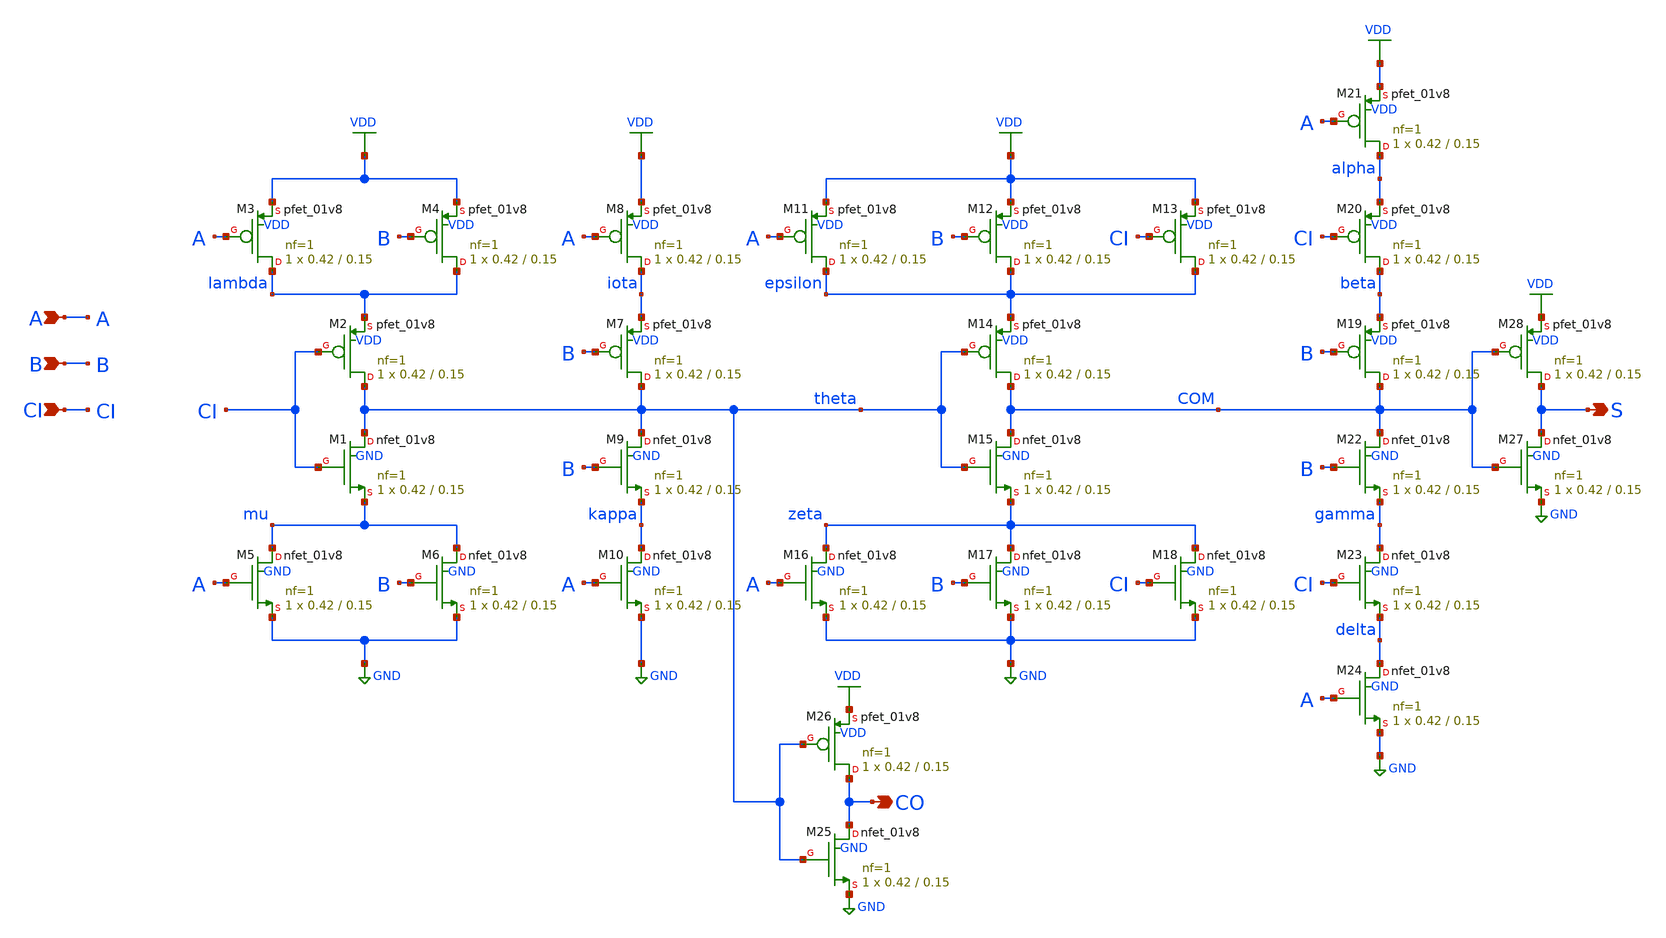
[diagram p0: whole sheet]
** sch_path: xschem/addf.sch
**.subckt addf A B CI S CO
*.ipin A
*.ipin B
*.ipin CI
*.opin S
*.opin CO
XM1 theta CI mu GND sky130_fd_pr__nfet_01v8 L=0.15 W=0.42 nf=1 ad='int((nf+1)/2) * W/nf * 0.29' as='int((nf+2)/2) * W/nf * 0.29'
+ pd='2*int((nf+1)/2) * (W/nf + 0.29)' ps='2*int((nf+2)/2) * (W/nf + 0.29)' nrd='0.29 / W' nrs='0.29 / W'
+ sa=0 sb=0 sd=0 mult=1 m=1
XM2 theta CI lambda VDD sky130_fd_pr__pfet_01v8 L=0.15 W=0.42 nf=1 ad='int((nf+1)/2) * W/nf * 0.29' as='int((nf+2)/2) * W/nf * 0.29'
+ pd='2*int((nf+1)/2) * (W/nf + 0.29)' ps='2*int((nf+2)/2) * (W/nf + 0.29)' nrd='0.29 / W' nrs='0.29 / W'
+ sa=0 sb=0 sd=0 mult=1 m=1
XM3 lambda A VDD VDD sky130_fd_pr__pfet_01v8 L=0.15 W=0.42 nf=1 ad='int((nf+1)/2) * W/nf * 0.29' as='int((nf+2)/2) * W/nf * 0.29'
+ pd='2*int((nf+1)/2) * (W/nf + 0.29)' ps='2*int((nf+2)/2) * (W/nf + 0.29)' nrd='0.29 / W' nrs='0.29 / W'
+ sa=0 sb=0 sd=0 mult=1 m=1
XM4 lambda B VDD VDD sky130_fd_pr__pfet_01v8 L=0.15 W=0.42 nf=1 ad='int((nf+1)/2) * W/nf * 0.29' as='int((nf+2)/2) * W/nf * 0.29'
+ pd='2*int((nf+1)/2) * (W/nf + 0.29)' ps='2*int((nf+2)/2) * (W/nf + 0.29)' nrd='0.29 / W' nrs='0.29 / W'
+ sa=0 sb=0 sd=0 mult=1 m=1
XM5 mu A GND GND sky130_fd_pr__nfet_01v8 L=0.15 W=0.42 nf=1 ad='int((nf+1)/2) * W/nf * 0.29' as='int((nf+2)/2) * W/nf * 0.29'
+ pd='2*int((nf+1)/2) * (W/nf + 0.29)' ps='2*int((nf+2)/2) * (W/nf + 0.29)' nrd='0.29 / W' nrs='0.29 / W'
+ sa=0 sb=0 sd=0 mult=1 m=1
XM6 mu B GND GND sky130_fd_pr__nfet_01v8 L=0.15 W=0.42 nf=1 ad='int((nf+1)/2) * W/nf * 0.29' as='int((nf+2)/2) * W/nf * 0.29'
+ pd='2*int((nf+1)/2) * (W/nf + 0.29)' ps='2*int((nf+2)/2) * (W/nf + 0.29)' nrd='0.29 / W' nrs='0.29 / W'
+ sa=0 sb=0 sd=0 mult=1 m=1
XM7 theta B iota VDD sky130_fd_pr__pfet_01v8 L=0.15 W=0.42 nf=1 ad='int((nf+1)/2) * W/nf * 0.29' as='int((nf+2)/2) * W/nf * 0.29'
+ pd='2*int((nf+1)/2) * (W/nf + 0.29)' ps='2*int((nf+2)/2) * (W/nf + 0.29)' nrd='0.29 / W' nrs='0.29 / W'
+ sa=0 sb=0 sd=0 mult=1 m=1
XM8 iota A VDD VDD sky130_fd_pr__pfet_01v8 L=0.15 W=0.42 nf=1 ad='int((nf+1)/2) * W/nf * 0.29' as='int((nf+2)/2) * W/nf * 0.29'
+ pd='2*int((nf+1)/2) * (W/nf + 0.29)' ps='2*int((nf+2)/2) * (W/nf + 0.29)' nrd='0.29 / W' nrs='0.29 / W'
+ sa=0 sb=0 sd=0 mult=1 m=1
XM9 theta B kappa GND sky130_fd_pr__nfet_01v8 L=0.15 W=0.42 nf=1 ad='int((nf+1)/2) * W/nf * 0.29' as='int((nf+2)/2) * W/nf * 0.29'
+ pd='2*int((nf+1)/2) * (W/nf + 0.29)' ps='2*int((nf+2)/2) * (W/nf + 0.29)' nrd='0.29 / W' nrs='0.29 / W'
+ sa=0 sb=0 sd=0 mult=1 m=1
XM10 kappa A GND GND sky130_fd_pr__nfet_01v8 L=0.15 W=0.42 nf=1 ad='int((nf+1)/2) * W/nf * 0.29' as='int((nf+2)/2) * W/nf * 0.29'
+ pd='2*int((nf+1)/2) * (W/nf + 0.29)' ps='2*int((nf+2)/2) * (W/nf + 0.29)' nrd='0.29 / W' nrs='0.29 / W'
+ sa=0 sb=0 sd=0 mult=1 m=1
XM11 epsilon A VDD VDD sky130_fd_pr__pfet_01v8 L=0.15 W=0.42 nf=1 ad='int((nf+1)/2) * W/nf * 0.29' as='int((nf+2)/2) * W/nf * 0.29'
+ pd='2*int((nf+1)/2) * (W/nf + 0.29)' ps='2*int((nf+2)/2) * (W/nf + 0.29)' nrd='0.29 / W' nrs='0.29 / W'
+ sa=0 sb=0 sd=0 mult=1 m=1
XM12 epsilon B VDD VDD sky130_fd_pr__pfet_01v8 L=0.15 W=0.42 nf=1 ad='int((nf+1)/2) * W/nf * 0.29' as='int((nf+2)/2) * W/nf * 0.29'
+ pd='2*int((nf+1)/2) * (W/nf + 0.29)' ps='2*int((nf+2)/2) * (W/nf + 0.29)' nrd='0.29 / W' nrs='0.29 / W'
+ sa=0 sb=0 sd=0 mult=1 m=1
XM13 epsilon CI VDD VDD sky130_fd_pr__pfet_01v8 L=0.15 W=0.42 nf=1 ad='int((nf+1)/2) * W/nf * 0.29' as='int((nf+2)/2) * W/nf * 0.29'
+ pd='2*int((nf+1)/2) * (W/nf + 0.29)' ps='2*int((nf+2)/2) * (W/nf + 0.29)' nrd='0.29 / W' nrs='0.29 / W'
+ sa=0 sb=0 sd=0 mult=1 m=1
XM14 COM theta epsilon VDD sky130_fd_pr__pfet_01v8 L=0.15 W=0.42 nf=1 ad='int((nf+1)/2) * W/nf * 0.29'
+ as='int((nf+2)/2) * W/nf * 0.29' pd='2*int((nf+1)/2) * (W/nf + 0.29)' ps='2*int((nf+2)/2) * (W/nf + 0.29)'
+ nrd='0.29 / W' nrs='0.29 / W' sa=0 sb=0 sd=0 mult=1 m=1
XM15 COM theta zeta GND sky130_fd_pr__nfet_01v8 L=0.15 W=0.42 nf=1 ad='int((nf+1)/2) * W/nf * 0.29' as='int((nf+2)/2) * W/nf * 0.29'
+ pd='2*int((nf+1)/2) * (W/nf + 0.29)' ps='2*int((nf+2)/2) * (W/nf + 0.29)' nrd='0.29 / W' nrs='0.29 / W'
+ sa=0 sb=0 sd=0 mult=1 m=1
XM16 zeta A GND GND sky130_fd_pr__nfet_01v8 L=0.15 W=0.42 nf=1 ad='int((nf+1)/2) * W/nf * 0.29' as='int((nf+2)/2) * W/nf * 0.29'
+ pd='2*int((nf+1)/2) * (W/nf + 0.29)' ps='2*int((nf+2)/2) * (W/nf + 0.29)' nrd='0.29 / W' nrs='0.29 / W'
+ sa=0 sb=0 sd=0 mult=1 m=1
XM17 zeta B GND GND sky130_fd_pr__nfet_01v8 L=0.15 W=0.42 nf=1 ad='int((nf+1)/2) * W/nf * 0.29' as='int((nf+2)/2) * W/nf * 0.29'
+ pd='2*int((nf+1)/2) * (W/nf + 0.29)' ps='2*int((nf+2)/2) * (W/nf + 0.29)' nrd='0.29 / W' nrs='0.29 / W'
+ sa=0 sb=0 sd=0 mult=1 m=1
XM18 zeta CI GND GND sky130_fd_pr__nfet_01v8 L=0.15 W=0.42 nf=1 ad='int((nf+1)/2) * W/nf * 0.29' as='int((nf+2)/2) * W/nf * 0.29'
+ pd='2*int((nf+1)/2) * (W/nf + 0.29)' ps='2*int((nf+2)/2) * (W/nf + 0.29)' nrd='0.29 / W' nrs='0.29 / W'
+ sa=0 sb=0 sd=0 mult=1 m=1
XM19 COM B beta VDD sky130_fd_pr__pfet_01v8 L=0.15 W=0.42 nf=1 ad='int((nf+1)/2) * W/nf * 0.29' as='int((nf+2)/2) * W/nf * 0.29'
+ pd='2*int((nf+1)/2) * (W/nf + 0.29)' ps='2*int((nf+2)/2) * (W/nf + 0.29)' nrd='0.29 / W' nrs='0.29 / W'
+ sa=0 sb=0 sd=0 mult=1 m=1
XM20 beta CI alpha VDD sky130_fd_pr__pfet_01v8 L=0.15 W=0.42 nf=1 ad='int((nf+1)/2) * W/nf * 0.29' as='int((nf+2)/2) * W/nf * 0.29'
+ pd='2*int((nf+1)/2) * (W/nf + 0.29)' ps='2*int((nf+2)/2) * (W/nf + 0.29)' nrd='0.29 / W' nrs='0.29 / W'
+ sa=0 sb=0 sd=0 mult=1 m=1
XM21 alpha A VDD VDD sky130_fd_pr__pfet_01v8 L=0.15 W=0.42 nf=1 ad='int((nf+1)/2) * W/nf * 0.29' as='int((nf+2)/2) * W/nf * 0.29'
+ pd='2*int((nf+1)/2) * (W/nf + 0.29)' ps='2*int((nf+2)/2) * (W/nf + 0.29)' nrd='0.29 / W' nrs='0.29 / W'
+ sa=0 sb=0 sd=0 mult=1 m=1
XM22 COM B gamma GND sky130_fd_pr__nfet_01v8 L=0.15 W=0.42 nf=1 ad='int((nf+1)/2) * W/nf * 0.29' as='int((nf+2)/2) * W/nf * 0.29'
+ pd='2*int((nf+1)/2) * (W/nf + 0.29)' ps='2*int((nf+2)/2) * (W/nf + 0.29)' nrd='0.29 / W' nrs='0.29 / W'
+ sa=0 sb=0 sd=0 mult=1 m=1
XM23 gamma CI delta GND sky130_fd_pr__nfet_01v8 L=0.15 W=0.42 nf=1 ad='int((nf+1)/2) * W/nf * 0.29' as='int((nf+2)/2) * W/nf * 0.29'
+ pd='2*int((nf+1)/2) * (W/nf + 0.29)' ps='2*int((nf+2)/2) * (W/nf + 0.29)' nrd='0.29 / W' nrs='0.29 / W'
+ sa=0 sb=0 sd=0 mult=1 m=1
XM24 delta A GND GND sky130_fd_pr__nfet_01v8 L=0.15 W=0.42 nf=1 ad='int((nf+1)/2) * W/nf * 0.29' as='int((nf+2)/2) * W/nf * 0.29'
+ pd='2*int((nf+1)/2) * (W/nf + 0.29)' ps='2*int((nf+2)/2) * (W/nf + 0.29)' nrd='0.29 / W' nrs='0.29 / W'
+ sa=0 sb=0 sd=0 mult=1 m=1
XM25 CO theta GND GND sky130_fd_pr__nfet_01v8 L=0.15 W=0.42 nf=1 ad='int((nf+1)/2) * W/nf * 0.29' as='int((nf+2)/2) * W/nf * 0.29'
+ pd='2*int((nf+1)/2) * (W/nf + 0.29)' ps='2*int((nf+2)/2) * (W/nf + 0.29)' nrd='0.29 / W' nrs='0.29 / W'
+ sa=0 sb=0 sd=0 mult=1 m=1
XM26 CO theta VDD VDD sky130_fd_pr__pfet_01v8 L=0.15 W=0.42 nf=1 ad='int((nf+1)/2) * W/nf * 0.29' as='int((nf+2)/2) * W/nf * 0.29'
+ pd='2*int((nf+1)/2) * (W/nf + 0.29)' ps='2*int((nf+2)/2) * (W/nf + 0.29)' nrd='0.29 / W' nrs='0.29 / W'
+ sa=0 sb=0 sd=0 mult=1 m=1
XM27 S COM GND GND sky130_fd_pr__nfet_01v8 L=0.15 W=0.42 nf=1 ad='int((nf+1)/2) * W/nf * 0.29' as='int((nf+2)/2) * W/nf * 0.29'
+ pd='2*int((nf+1)/2) * (W/nf + 0.29)' ps='2*int((nf+2)/2) * (W/nf + 0.29)' nrd='0.29 / W' nrs='0.29 / W'
+ sa=0 sb=0 sd=0 mult=1 m=1
XM28 S COM VDD VDD sky130_fd_pr__pfet_01v8 L=0.15 W=0.42 nf=1 ad='int((nf+1)/2) * W/nf * 0.29' as='int((nf+2)/2) * W/nf * 0.29'
+ pd='2*int((nf+1)/2) * (W/nf + 0.29)' ps='2*int((nf+2)/2) * (W/nf + 0.29)' nrd='0.29 / W' nrs='0.29 / W'
+ sa=0 sb=0 sd=0 mult=1 m=1
**.ends
.GLOBAL VDD
.GLOBAL GND
.end
